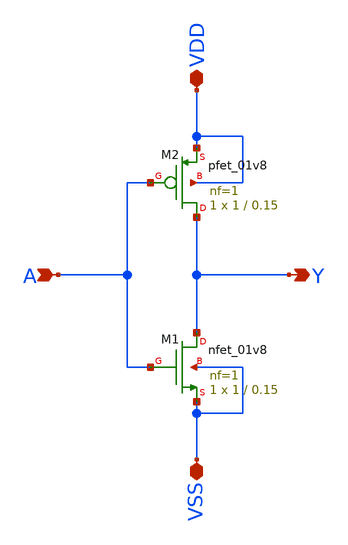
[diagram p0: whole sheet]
** sch_path: inverter/inverter.sch
**.subckt inverter VDD VSS A Y
*.iopin VDD
*.iopin VSS
*.ipin A
*.opin Y
XM1 Y A VSS VSS sky130_fd_pr__nfet_01v8 L=0.15 W=1 nf=1 ad='int((1 + 1)/2) * 1 / 1 * 0.29' as='int((1 + 2)/2) * 1 / 1 * 0.29'
+ pd='2*int((1 + 1)/2) * (1 / 1 + 0.29)' ps='2*int((1 + 2)/2) * (1 / 1 + 0.29)' nrd='0.29 / 1 ' nrs='0.29 / 1 '
+ sa=0 sb=0 sd=0 mult=1 m=1
XM2 Y A VDD VDD sky130_fd_pr__pfet_01v8 L=0.15 W=1 nf=1 ad='int((1 + 1)/2) * 1 / 1 * 0.29' as='int((1 + 2)/2) * 1 / 1 * 0.29'
+ pd='2*int((1 + 1)/2) * (1 / 1 + 0.29)' ps='2*int((1 + 2)/2) * (1 / 1 + 0.29)' nrd='0.29 / 1 ' nrs='0.29 / 1 '
+ sa=0 sb=0 sd=0 mult=1 m=1
**.ends
.end
